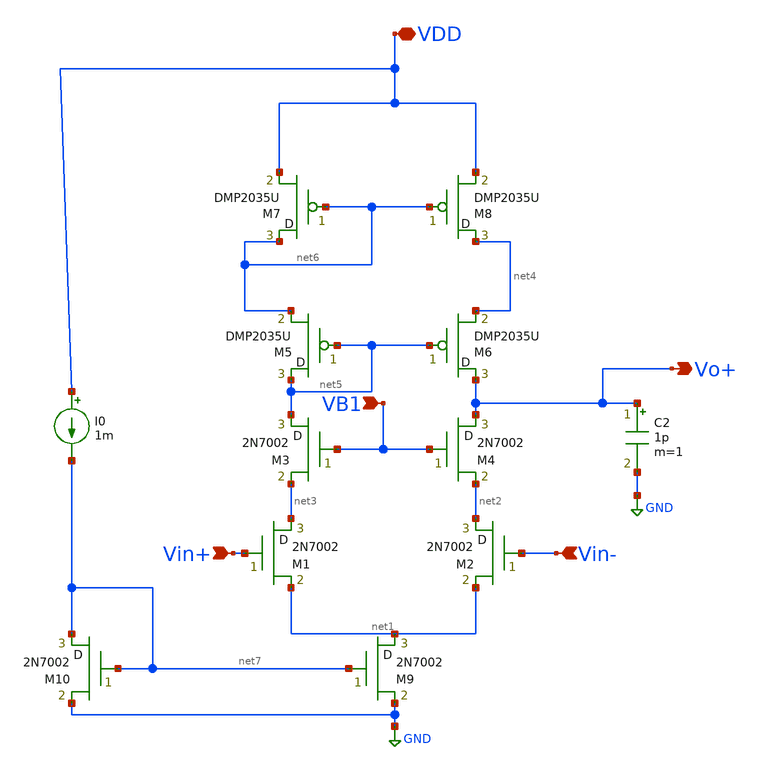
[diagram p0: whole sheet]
** sch_path: OTA9T.sch
**.subckt OTA9T Vin+ Vin- Vo+ VDD VB1
*.ipin Vin+
*.ipin Vin-
*.opin Vo+
*.iopin VDD
*.ipin VB1
M1 net3 Vin+ net1 M2N7002 m=1
M2 net2 Vin- net1 M2N7002 m=1
M3 net5 VB1 net3 M2N7002 m=1
M4 Vo+ VB1 net2 M2N7002 m=1
M6 Vo+ net5 net4 DMP2035U m=1
M5 net5 net5 net6 DMP2035U m=1
M7 net6 net6 VDD DMP2035U m=1
M8 net4 net6 VDD DMP2035U m=1
M9 net1 net7 GND M2N7002 m=1
C2 Vo+ GND 1p m=1
M10 net7 net7 GND M2N7002 m=1
I0 VDD net7 1m
**.ends
.GLOBAL GND
.end
